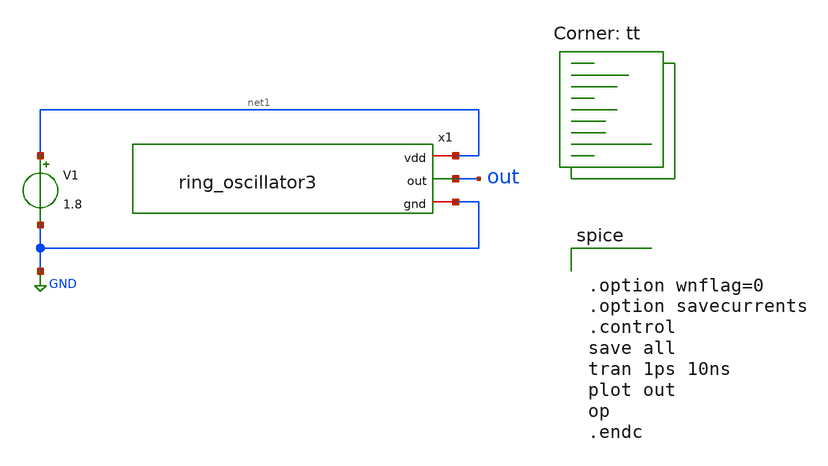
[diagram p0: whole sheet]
** sch_path: iinverter/ring_oscillator3_tb.sch
**.subckt ring_oscillator3_tb
x1 net1 out GND ring_oscillator3
V1 net1 GND 1.8
**** begin user architecture code
.lib $::SKYWATER_MODELS/sky130.lib.spice tt


.option wnflag=0
.option savecurrents
.control
save all
tran 1ps 10ns
plot out
op
.endc


**** end user architecture code
**.ends

* expanding   symbol:  ring_oscillator3.sym # of pins=3
** sym_path: iinverter/ring_oscillator3.sym
** sch_path: iinverter/ring_oscillator3.sch
.subckt ring_oscillator3 vdd out gnd
*.iopin vdd
*.opin out
*.iopin gnd
x1 vdd net1 net2 gnd iinverter
x2 vdd net2 out gnd iinverter
x3 vdd out net1 gnd iinverter
.ends


* expanding   symbol:  iinverter.sym # of pins=4
** sym_path: iinverter/iinverter.sym
** sch_path: iinverter/iinverter.sch
.subckt iinverter vvdd in out vgnd
*.ipin vvdd
*.ipin in
*.ipin vgnd
*.opin out
XM3 out in vgnd vgnd sky130_fd_pr__nfet_01v8 L=0.15 W=1 nf=1 ad='int((nf+1)/2) * W/nf * 0.29' as='int((nf+2)/2) * W/nf * 0.29'
+ pd='2*int((nf+1)/2) * (W/nf + 0.29)' ps='2*int((nf+2)/2) * (W/nf + 0.29)' nrd='0.29 / W' nrs='0.29 / W'
+ sa=0 sb=0 sd=0 mult=1 m=1
XM2 out in vvdd vvdd sky130_fd_pr__pfet_01v8 L=0.15 W=1 nf=1 ad='int((nf+1)/2) * W/nf * 0.29' as='int((nf+2)/2) * W/nf * 0.29'
+ pd='2*int((nf+1)/2) * (W/nf + 0.29)' ps='2*int((nf+2)/2) * (W/nf + 0.29)' nrd='0.29 / W' nrs='0.29 / W'
+ sa=0 sb=0 sd=0 mult=1 m=1
.ends

.GLOBAL GND
.end
